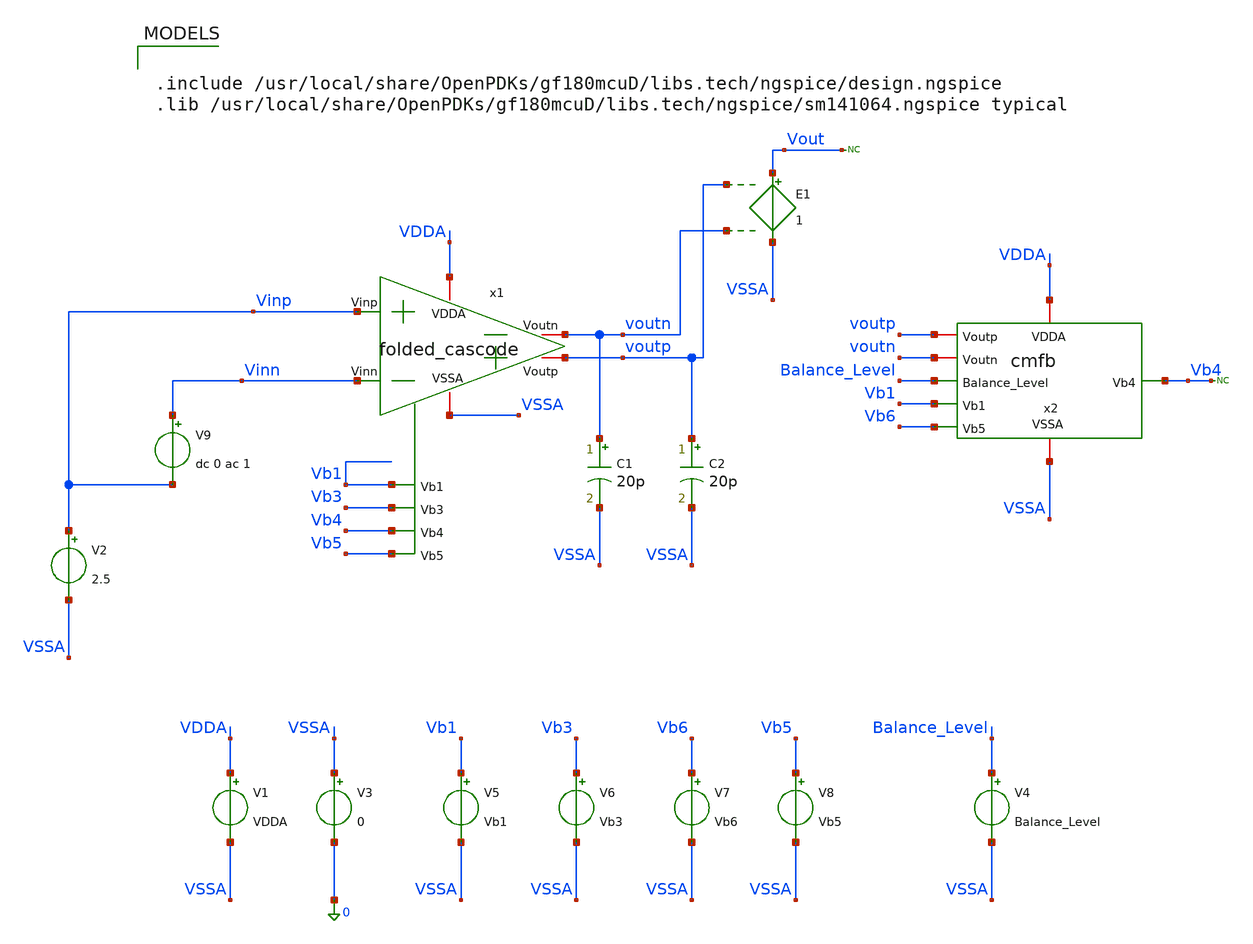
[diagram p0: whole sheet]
** sch_path: Folded_cascode/testbenches/simulation/fc_cmfb_ac_tb_batch.sch
**.subckt fc_cmfb_ac_tb_batch
x1 VDDA VSSA Vinp Vinn voutp voutn Vb1 Vb3 Vb4 Vb5 folded_cascode
x2 VDDA VSSA voutp voutn Balance_Level Vb1 Vb4 Vb6 cmfb
V2 Vinp VSSA 2.5
C1 voutn VSSA 20p m=1
C2 voutp VSSA 20p m=1
V1 VDDA VSSA VDDA
V3 VSSA 0 0
V5 Vb1 VSSA Vb1
V6 Vb3 VSSA Vb3
V4 Balance_Level VSSA Balance_Level
* noconn Vb4
E1 Vout VSSA voutp voutn 1
* noconn Vout
V9 Vinn Vinp dc 0 ac 1
V8 Vb5 VSSA Vb5
V7 Vb6 VSSA Vb6
**** begin user architecture code

.include /usr/local/share/OpenPDKs/gf180mcuD/libs.tech/ngspice/design.ngspice
.lib /usr/local/share/OpenPDKs/gf180mcuD/libs.tech/ngspice/sm141064.ngspice typical



.temp 27
.param VDDA = 5
.param Balance_Level = 1.3
.param Vb1 = 3.96
.param Vb3 = 3.6
.param Vb5 = 0.72
.param Vb6 = 0.83
.param VD = 0

.control
option sparse
set filetype=ascii
set wr_singlescale
set wr_vecnames
save all
save @m.x1.xm1.m0[id]
save @m.x1.xm1.m0[gm]
save @m.x1.xm1.m0[vgs]
save @m.x1.xm1.m0[vds]
save @m.x1.xm1.m0[vth]
save @m.x1.xm1.m0[gds]

save @m.x1.xm2.m0[id]
save @m.x1.xm2.m0[gm]
save @m.x1.xm2.m0[vgs]
save @m.x1.xm2.m0[vds]
save @m.x1.xm2.m0[vth]
save @m.x1.xm2.m0[gds]

save @m.x1.xm9.m0[id]
save @m.x1.xm9.m0[gm]
save @m.x1.xm9.m0[vgs]
save @m.x1.xm9.m0[vds]
save @m.x1.xm9.m0[vth]
save @m.x1.xm9.m0[gds]

save @m.x1.xm8.m0[id]
save @m.x1.xm8.m0[gm]
save @m.x1.xm8.m0[vgs]
save @m.x1.xm8.m0[vds]
save @m.x1.xm8.m0[vth]
save @m.x1.xm8.m0[gds]

save @m.x1.xm6.m0[id]
save @m.x1.xm6.m0[gm]
save @m.x1.xm6.m0[vgs]
save @m.x1.xm6.m0[vds]
save @m.x1.xm6.m0[vth]
save @m.x1.xm6.m0[gds]

save @m.x1.xm5.m0[id]
save @m.x1.xm5.m0[gm]
save @m.x1.xm5.m0[vgs]
save @m.x1.xm5.m0[vds]
save @m.x1.xm5.m0[vth]
save @m.x1.xm5.m0[gds]
save @m.x1.xm5.m0[vdsat]
save @m.x1.xm4.m0[vdsat]

save @m.x2.xm1.m0[id]
save @m.x2.xm1.m0[gm]
save @m.x2.xm1.m0[vgs]
save @m.x2.xm1.m0[vds]
save @m.x2.xm1.m0[vth]
save @m.x2.xm1.m0[gds]

save @m.x2.xm2.m0[id]
save @m.x2.xm2.m0[gm]
save @m.x2.xm2.m0[vgs]
save @m.x2.xm2.m0[vds]
save @m.x2.xm2.m0[vth]
save @m.x2.xm2.m0[gds]

save @m.x2.xm3.m0[id]
save @m.x2.xm3.m0[gm]
save @m.x2.xm3.m0[vgs]
save @m.x2.xm3.m0[vds]
save @m.x2.xm3.m0[vth]
save @m.x2.xm3.m0[gds]

save @m.x2.xm4.m0[id]
save @m.x2.xm4.m0[gm]
save @m.x2.xm4.m0[vgs]
save @m.x2.xm4.m0[vds]
save @m.x2.xm4.m0[vth]
save @m.x2.xm4.m0[gds]

save @m.x2.xm5.m0[id]
save @m.x2.xm5.m0[gm]
save @m.x2.xm5.m0[vgs]
save @m.x2.xm5.m0[vds]
save @m.x2.xm5.m0[vth]
save @m.x2.xm5.m0[gds]

save @m.x2.xm6.m0[id]
save @m.x2.xm6.m0[gm]
save @m.x2.xm6.m0[vgs]
save @m.x2.xm6.m0[vds]
save @m.x2.xm6.m0[vth]
save @m.x2.xm6.m0[gds]

save @m.x2.xm7.m0[id]
save @m.x2.xm7.m0[gm]
save @m.x2.xm7.m0[vgs]
save @m.x2.xm7.m0[vds]
save @m.x2.xm7.m0[vth]
save @m.x2.xm7.m0[gds]

save @m.x2.xm8.m0[id]
save @m.x2.xm8.m0[gm]
save @m.x2.xm8.m0[vgs]
save @m.x2.xm8.m0[vds]
save @m.x2.xm8.m0[vth]
save @m.x2.xm8.m0[gds]

save @m.x2.xm9.m0[id]
save @m.x2.xm9.m0[gm]
save @m.x2.xm9.m0[vgs]
save @m.x2.xm9.m0[vds]
save @m.x2.xm9.m0[vth]
save @m.x2.xm9.m0[gds]

op

write fc_cmfb_op_tb.raw

set appendwrite
ac dec 100 1 1G

* Differential input/output
let vid = v(vinp) - v(vinn)
let vod = v(voutp) - v(voutn)

* Differential gain
let ad = vod / vid

* Magnitude and phase
let gain_db = db(ad)
let phase_deg = (180/pi)*ph(ad)

* Plots
plot gain_db
plot phase_deg

* DC / low-frequency gain
meas ac gain_dc FIND gain_db AT=1

* Unity-gain frequency
meas ac fu WHEN gain_db=0 CROSS=1

* Phase at unity gain
meas ac phase_fu FIND phase_deg AT=fu

* Phase margin
let pm = 180 + phase_fu

print gain_dc
print fu
print phase_fu
print pm

write fc_cmfb_ac_tb.raw

.endc


**** end user architecture code
**.ends
.end
